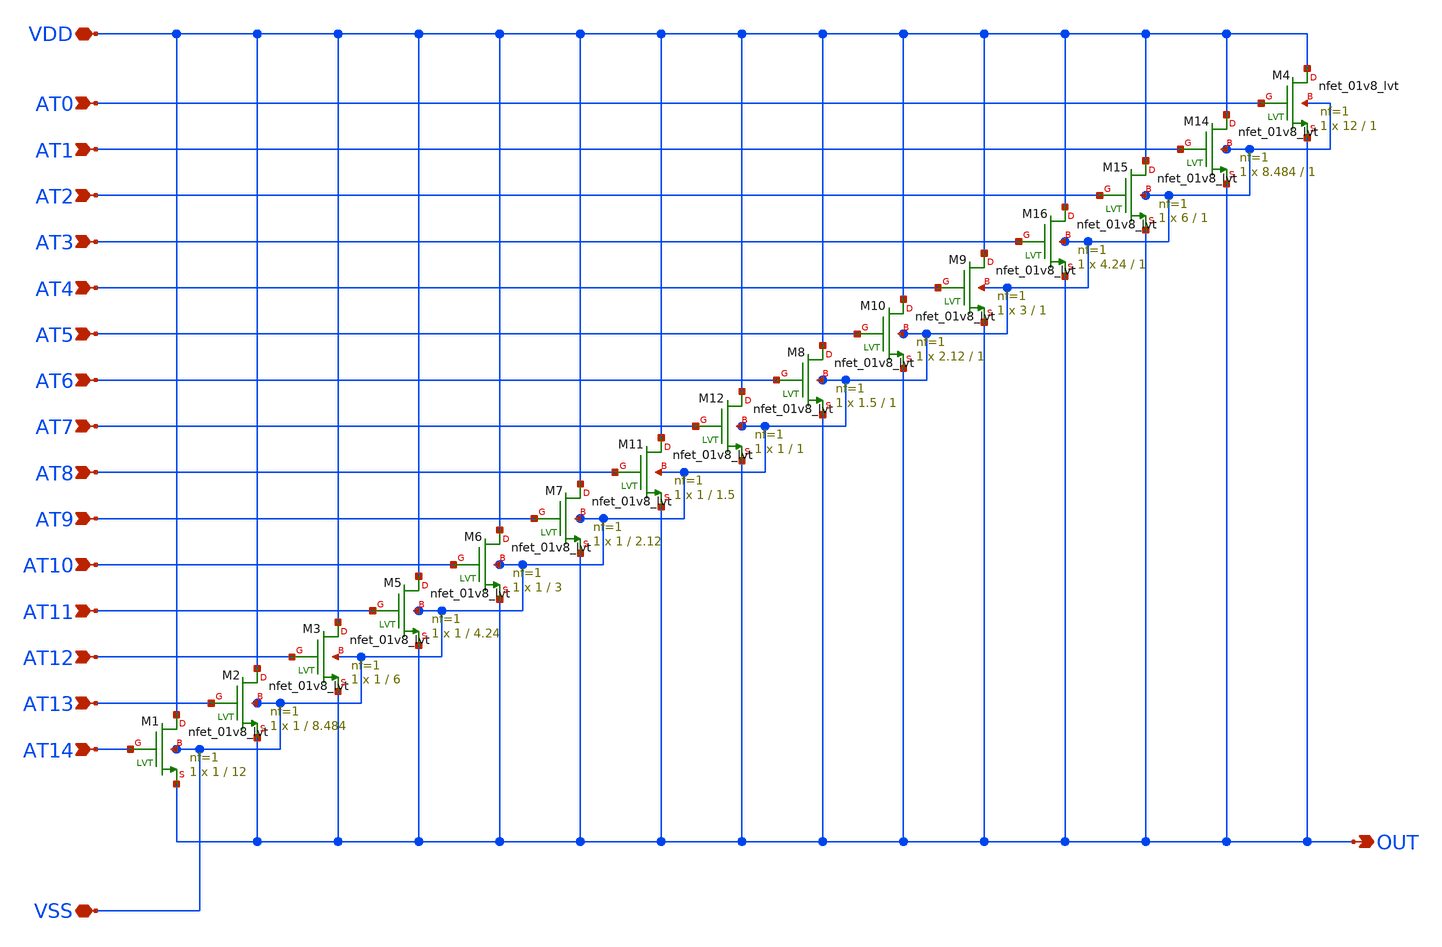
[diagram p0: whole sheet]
** sch_path: xschem/dac_16nfet.sch
**.subckt dac_16nfet AT12 AT13 VDD VSS OUT AT14 AT4 AT5 AT6 AT7 AT8 AT9 AT10 AT11 AT0 AT1 AT2 AT3
*.ipin AT12
*.ipin AT13
*.iopin VDD
*.iopin VSS
*.opin OUT
*.ipin AT14
*.ipin AT4
*.ipin AT5
*.ipin AT6
*.ipin AT7
*.ipin AT8
*.ipin AT9
*.ipin AT10
*.ipin AT11
*.ipin AT0
*.ipin AT1
*.ipin AT2
*.ipin AT3
XM4 VDD AT0 OUT VSS sky130_fd_pr__nfet_01v8_lvt L=1 W=12 nf=1 ad='int((nf+1)/2) * W/nf * 0.29' as='int((nf+2)/2) * W/nf * 0.29'
+ pd='2*int((nf+1)/2) * (W/nf + 0.29)' ps='2*int((nf+2)/2) * (W/nf + 0.29)' nrd='0.29 / W' nrs='0.29 / W'
+ sa=0 sb=0 sd=0 mult=1 m=1
XM14 VDD AT1 OUT VSS sky130_fd_pr__nfet_01v8_lvt L=1 W=8.484 nf=1 ad='int((nf+1)/2) * W/nf * 0.29' as='int((nf+2)/2) * W/nf * 0.29'
+ pd='2*int((nf+1)/2) * (W/nf + 0.29)' ps='2*int((nf+2)/2) * (W/nf + 0.29)' nrd='0.29 / W' nrs='0.29 / W'
+ sa=0 sb=0 sd=0 mult=1 m=1
XM15 VDD AT2 OUT VSS sky130_fd_pr__nfet_01v8_lvt L=1 W=6 nf=1 ad='int((nf+1)/2) * W/nf * 0.29' as='int((nf+2)/2) * W/nf * 0.29'
+ pd='2*int((nf+1)/2) * (W/nf + 0.29)' ps='2*int((nf+2)/2) * (W/nf + 0.29)' nrd='0.29 / W' nrs='0.29 / W'
+ sa=0 sb=0 sd=0 mult=1 m=1
XM16 VDD AT3 OUT VSS sky130_fd_pr__nfet_01v8_lvt L=1 W=4.24 nf=1 ad='int((nf+1)/2) * W/nf * 0.29' as='int((nf+2)/2) * W/nf * 0.29'
+ pd='2*int((nf+1)/2) * (W/nf + 0.29)' ps='2*int((nf+2)/2) * (W/nf + 0.29)' nrd='0.29 / W' nrs='0.29 / W'
+ sa=0 sb=0 sd=0 mult=1 m=1
XM9 VDD AT4 OUT VSS sky130_fd_pr__nfet_01v8_lvt L=1 W=3 nf=1 ad='int((nf+1)/2) * W/nf * 0.29' as='int((nf+2)/2) * W/nf * 0.29'
+ pd='2*int((nf+1)/2) * (W/nf + 0.29)' ps='2*int((nf+2)/2) * (W/nf + 0.29)' nrd='0.29 / W' nrs='0.29 / W'
+ sa=0 sb=0 sd=0 mult=1 m=1
XM10 VDD AT5 OUT VSS sky130_fd_pr__nfet_01v8_lvt L=1 W=2.12 nf=1 ad='int((nf+1)/2) * W/nf * 0.29' as='int((nf+2)/2) * W/nf * 0.29'
+ pd='2*int((nf+1)/2) * (W/nf + 0.29)' ps='2*int((nf+2)/2) * (W/nf + 0.29)' nrd='0.29 / W' nrs='0.29 / W'
+ sa=0 sb=0 sd=0 mult=1 m=1
XM12 VDD AT7 OUT VSS sky130_fd_pr__nfet_01v8_lvt L=1 W=1 nf=1 ad='int((nf+1)/2) * W/nf * 0.29' as='int((nf+2)/2) * W/nf * 0.29'
+ pd='2*int((nf+1)/2) * (W/nf + 0.29)' ps='2*int((nf+2)/2) * (W/nf + 0.29)' nrd='0.29 / W' nrs='0.29 / W'
+ sa=0 sb=0 sd=0 mult=1 m=1
XM1 VDD AT14 OUT VSS sky130_fd_pr__nfet_01v8_lvt L=12 W=1 nf=1 ad='int((nf+1)/2) * W/nf * 0.29' as='int((nf+2)/2) * W/nf * 0.29'
+ pd='2*int((nf+1)/2) * (W/nf + 0.29)' ps='2*int((nf+2)/2) * (W/nf + 0.29)' nrd='0.29 / W' nrs='0.29 / W'
+ sa=0 sb=0 sd=0 mult=1 m=1
XM2 VDD AT13 OUT VSS sky130_fd_pr__nfet_01v8_lvt L=8.484 W=1 nf=1 ad='int((nf+1)/2) * W/nf * 0.29' as='int((nf+2)/2) * W/nf * 0.29'
+ pd='2*int((nf+1)/2) * (W/nf + 0.29)' ps='2*int((nf+2)/2) * (W/nf + 0.29)' nrd='0.29 / W' nrs='0.29 / W'
+ sa=0 sb=0 sd=0 mult=1 m=1
XM3 VDD AT12 OUT VSS sky130_fd_pr__nfet_01v8_lvt L=6 W=1 nf=1 ad='int((nf+1)/2) * W/nf * 0.29' as='int((nf+2)/2) * W/nf * 0.29'
+ pd='2*int((nf+1)/2) * (W/nf + 0.29)' ps='2*int((nf+2)/2) * (W/nf + 0.29)' nrd='0.29 / W' nrs='0.29 / W'
+ sa=0 sb=0 sd=0 mult=1 m=1
XM5 VDD AT11 OUT VSS sky130_fd_pr__nfet_01v8_lvt L=4.24 W=1 nf=1 ad='int((nf+1)/2) * W/nf * 0.29' as='int((nf+2)/2) * W/nf * 0.29'
+ pd='2*int((nf+1)/2) * (W/nf + 0.29)' ps='2*int((nf+2)/2) * (W/nf + 0.29)' nrd='0.29 / W' nrs='0.29 / W'
+ sa=0 sb=0 sd=0 mult=1 m=1
XM6 VDD AT10 OUT VSS sky130_fd_pr__nfet_01v8_lvt L=3 W=1 nf=1 ad='int((nf+1)/2) * W/nf * 0.29' as='int((nf+2)/2) * W/nf * 0.29'
+ pd='2*int((nf+1)/2) * (W/nf + 0.29)' ps='2*int((nf+2)/2) * (W/nf + 0.29)' nrd='0.29 / W' nrs='0.29 / W'
+ sa=0 sb=0 sd=0 mult=1 m=1
XM7 VDD AT9 OUT VSS sky130_fd_pr__nfet_01v8_lvt L=2.12 W=1 nf=1 ad='int((nf+1)/2) * W/nf * 0.29' as='int((nf+2)/2) * W/nf * 0.29'
+ pd='2*int((nf+1)/2) * (W/nf + 0.29)' ps='2*int((nf+2)/2) * (W/nf + 0.29)' nrd='0.29 / W' nrs='0.29 / W'
+ sa=0 sb=0 sd=0 mult=1 m=1
XM8 VDD AT6 OUT VSS sky130_fd_pr__nfet_01v8_lvt L=1 W=1.5 nf=1 ad='int((nf+1)/2) * W/nf * 0.29' as='int((nf+2)/2) * W/nf * 0.29'
+ pd='2*int((nf+1)/2) * (W/nf + 0.29)' ps='2*int((nf+2)/2) * (W/nf + 0.29)' nrd='0.29 / W' nrs='0.29 / W'
+ sa=0 sb=0 sd=0 mult=1 m=1
XM11 VDD AT8 OUT VSS sky130_fd_pr__nfet_01v8_lvt L=1.5 W=1 nf=1 ad='int((nf+1)/2) * W/nf * 0.29' as='int((nf+2)/2) * W/nf * 0.29'
+ pd='2*int((nf+1)/2) * (W/nf + 0.29)' ps='2*int((nf+2)/2) * (W/nf + 0.29)' nrd='0.29 / W' nrs='0.29 / W'
+ sa=0 sb=0 sd=0 mult=1 m=1
**.ends
.end
